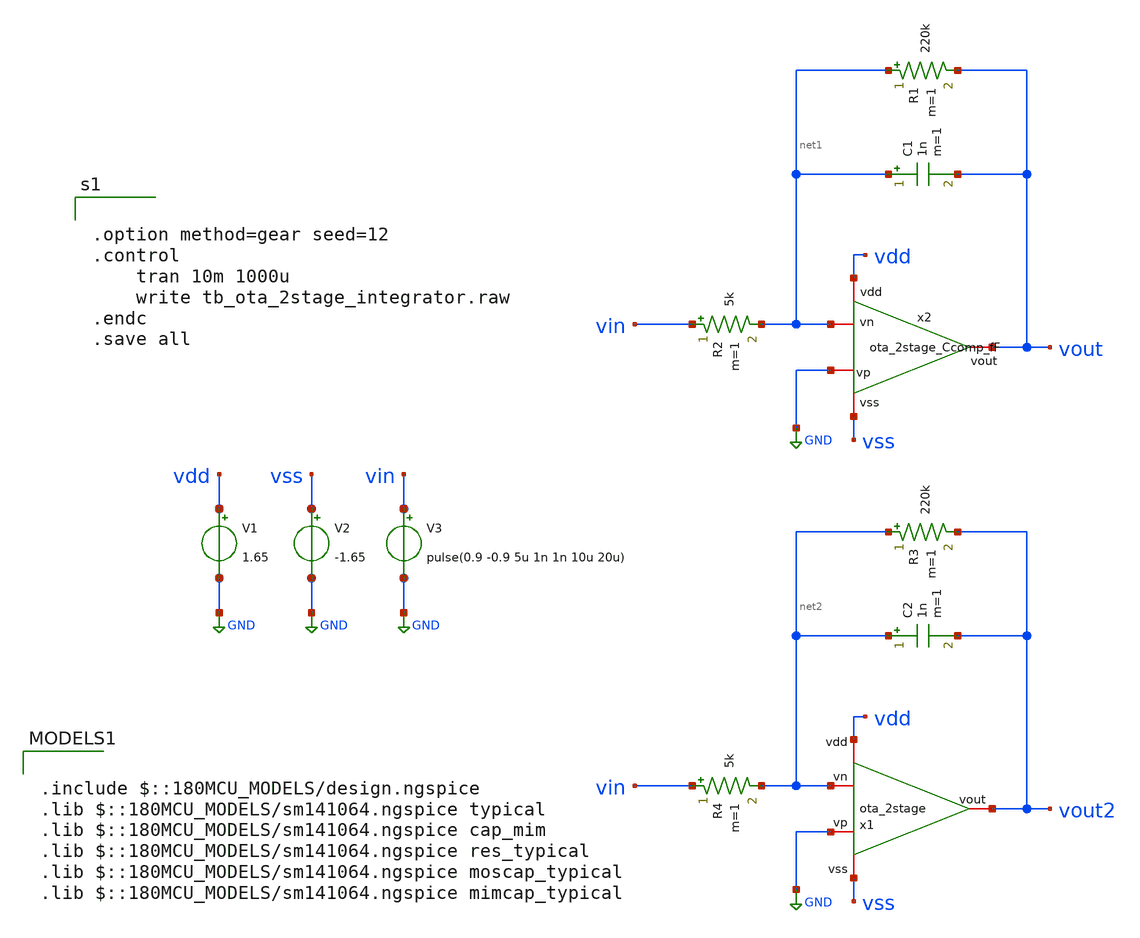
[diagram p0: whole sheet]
** sch_path: designs/libs/core_LIF_comp/tb_ota_2stage/tb_ota_2stage_integrator.sch
**.subckt tb_ota_2stage_integrator
x2 vdd vss GND vout net1 ota_2stage_Ccomp_fF
V1 vdd GND 1.65
V3 vin GND pulse(0.9 -0.9 5u 1n 1n 10u 20u)
R1 net1 vout 220k m=1
C1 net1 vout 1n m=1
R2 vin net1 5k m=1
V2 vss GND -1.65
R3 net2 vout2 220k m=1
C2 net2 vout2 1n m=1
R4 vin net2 5k m=1
x1 vdd net2 vout2 GND vss ota_2stage
**** begin user architecture code


.option method=gear seed=12
.control
    tran 10m 1000u
    write tb_ota_2stage_integrator.raw
.endc
.save all



.include $::180MCU_MODELS/design.ngspice
.lib $::180MCU_MODELS/sm141064.ngspice typical
.lib $::180MCU_MODELS/sm141064.ngspice cap_mim
.lib $::180MCU_MODELS/sm141064.ngspice res_typical
.lib $::180MCU_MODELS/sm141064.ngspice moscap_typical
.lib $::180MCU_MODELS/sm141064.ngspice mimcap_typical

**** end user architecture code
**.ends
.GLOBAL GND
.end
